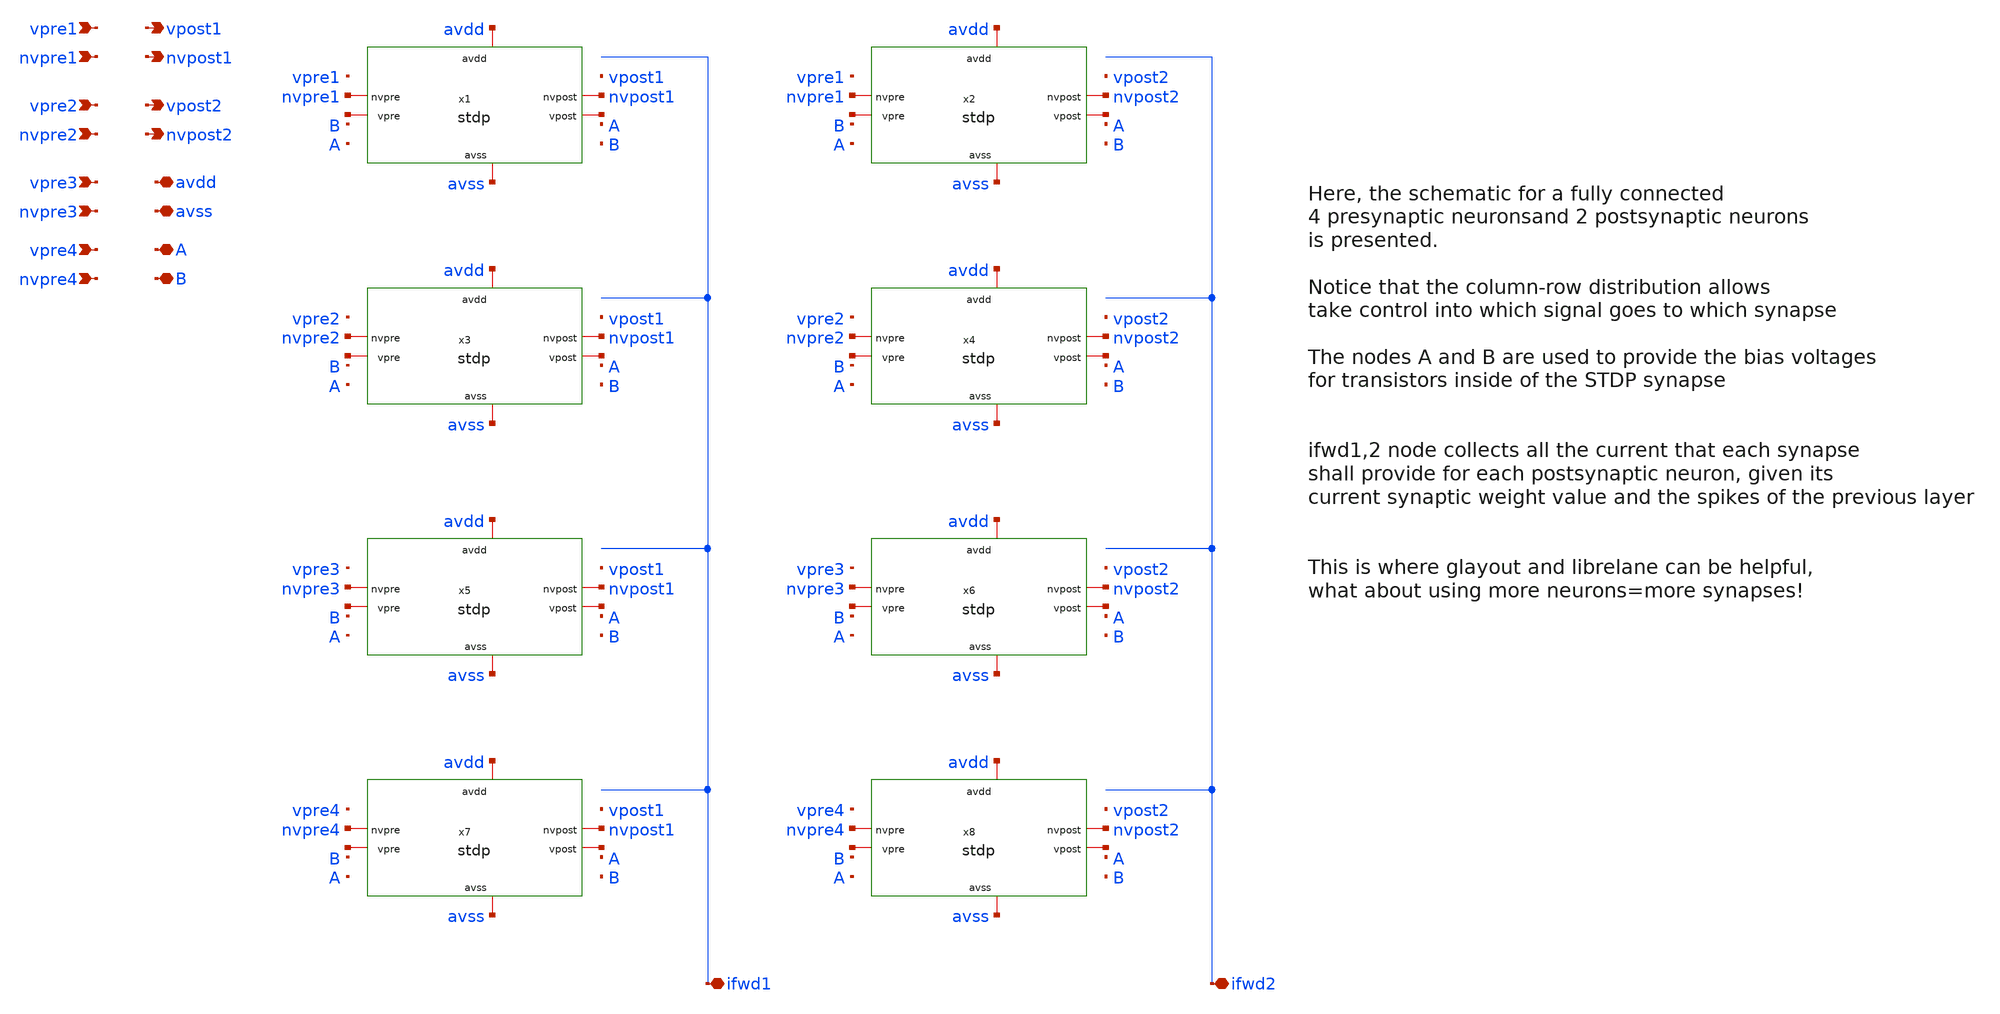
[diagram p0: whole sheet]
** sch_path: sch/stdp/stdp_4x2.sch
**.subckt stdp_4x2 ifwd1 ifwd2 vpre1 nvpre1 vpre2 nvpre2 vpre3 nvpre3 vpre4 nvpre4 vpost1 nvpost1
*+ vpost2 nvpost2 avdd avss A B
*.iopin ifwd1
*.iopin ifwd2
*.ipin vpre1
*.ipin nvpre1
*.ipin vpre2
*.ipin nvpre2
*.ipin vpre3
*.ipin nvpre3
*.ipin vpre4
*.ipin nvpre4
*.opin vpost1
*.opin nvpost1
*.opin vpost2
*.opin nvpost2
*.iopin avdd
*.iopin avss
*.iopin A
*.iopin B
x1 avdd avss nvpre1 nvpost1 net1 net2 stdp
x2 avdd avss nvpre1 nvpost2 net3 net4 stdp
x3 avdd avss nvpre2 nvpost1 net5 net6 stdp
x4 avdd avss nvpre2 nvpost2 net7 net8 stdp
x5 avdd avss nvpre3 nvpost1 net9 net10 stdp
x6 avdd avss nvpre3 nvpost2 net11 net12 stdp
x7 avdd avss nvpre4 nvpost1 net13 net14 stdp
x8 avdd avss nvpre4 nvpost2 net15 net16 stdp
**.ends
.end
